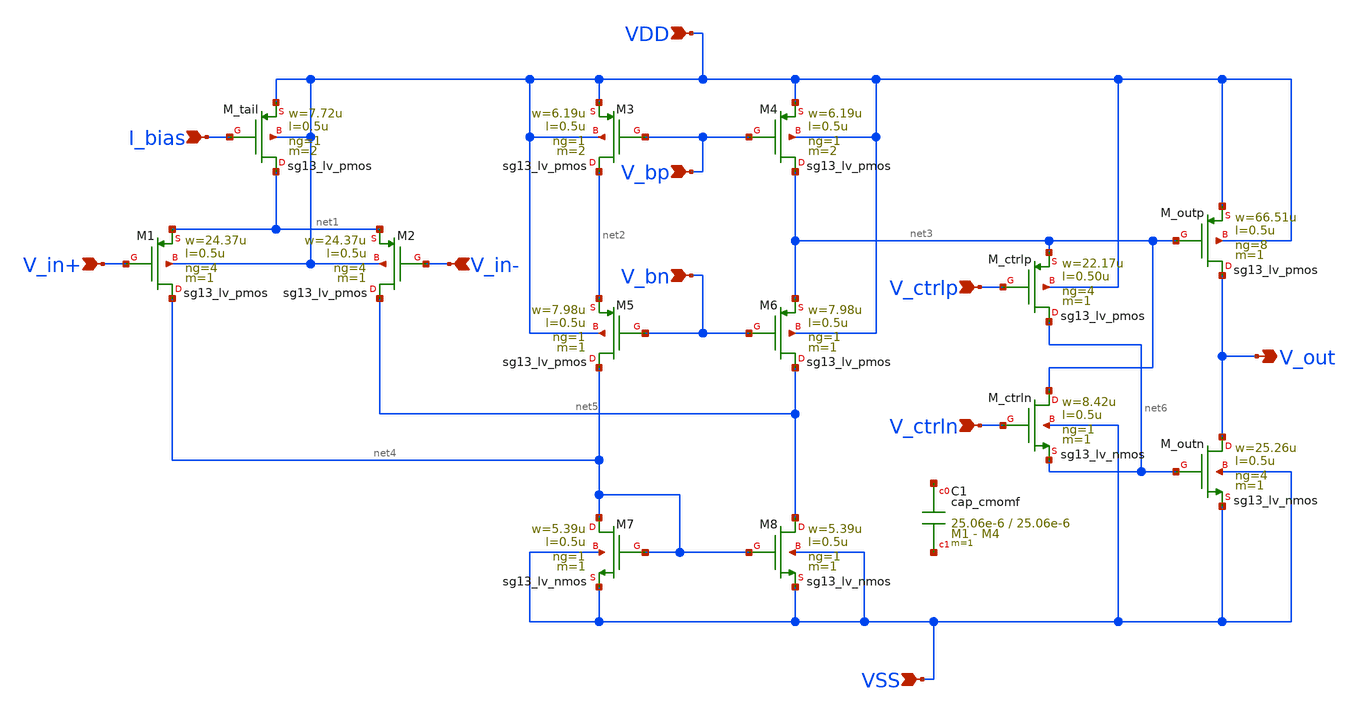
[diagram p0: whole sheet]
** sch_path: designs/libs/core_analog/coarse_gain/coarse_gain_ota.sch
**.subckt coarse_gain_ota I_bias V_in+ V_in- V_bp V_bn V_ctrlp V_ctrln VDD VSS V_out
*.ipin I_bias
*.ipin V_in+
*.ipin V_in-
*.ipin V_bp
*.ipin V_bn
*.ipin V_ctrlp
*.ipin V_ctrln
*.ipin VDD
*.ipin VSS
*.opin V_out
XM1 net4 V_in+ net1 VDD sg13_lv_pmos w=24.37u l=0.5u ng=4 m=1 mm_ok=1
XM2 net5 V_in- net1 VDD sg13_lv_pmos w=24.37u l=0.5u ng=4 m=1 mm_ok=1
XM3 net2 V_bp VDD VDD sg13_lv_pmos w=6.19u l=0.5u ng=1 m=2 mm_ok=1
XM4 net3 V_bp VDD VDD sg13_lv_pmos w=6.19u l=0.5u ng=1 m=2 mm_ok=1
XM5 net4 V_bn net2 VDD sg13_lv_pmos w=7.98u l=0.5u ng=1 m=1 mm_ok=1
XM6 net5 V_bn net3 VDD sg13_lv_pmos w=7.98u l=0.5u ng=1 m=1 mm_ok=1
XM7 net4 net4 VSS VSS sg13_lv_nmos w=5.39u l=0.5u ng=1 m=1 mm_ok=1
XM8 net5 net4 VSS VSS sg13_lv_nmos w=5.39u l=0.5u ng=1 m=1 mm_ok=1
XM_tail net1 I_bias VDD VDD sg13_lv_pmos w=7.72u l=0.5u ng=1 m=2 mm_ok=1
XM_ctrlp net6 V_ctrlp net3 VDD sg13_lv_pmos w=22.17u l=0.50u ng=4 m=1 mm_ok=1
XM_outp V_out net3 VDD VDD sg13_lv_pmos w=66.51u l=0.5u ng=8 m=1 mm_ok=1
XM_ctrln net3 V_ctrln net6 VSS sg13_lv_nmos w=8.42u l=0.5u ng=1 m=1 mm_ok=1
XM_outn V_out net6 VSS VSS sg13_lv_nmos w=25.26u l=0.5u ng=4 m=1 mm_ok=1
XC1 net7 net8 cap_cmomf w=25.06e-6 l=25.06e-6 mmin=1 mmax=4 subblock=0 rfmodel=0 subscale=1 m=1
+ mm_ok=1
**.ends
.end
